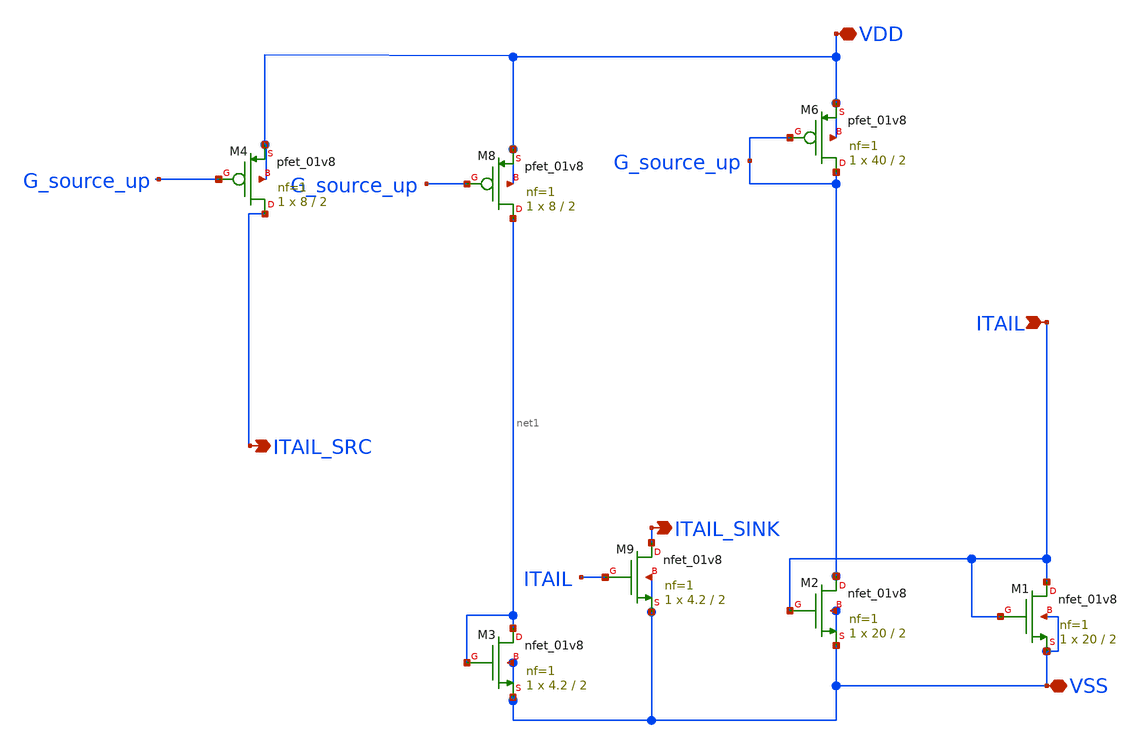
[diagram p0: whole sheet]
** sch_path: Xschem/PLL_TOP_Schematics/Current_Mirror_Top_s.sch
**.subckt Current_Mirror_Top_s ITAIL VDD VSS ITAIL_SRC ITAIL_SINK
*.ipin ITAIL
*.iopin VDD
*.iopin VSS
*.opin ITAIL_SRC
*.opin ITAIL_SINK
XM8 net1 G_source_up VDD VDD sky130_fd_pr__pfet_01v8 L=2 W=8 nf=1 ad='int((nf+1)/2) * W/nf * 0.29' as='int((nf+2)/2) * W/nf * 0.29'
+ pd='2*int((nf+1)/2) * (W/nf + 0.29)' ps='2*int((nf+2)/2) * (W/nf + 0.29)' nrd='0.29 / W' nrs='0.29 / W'
+ sa=0 sb=0 sd=0 mult=1 m=1
XM6 G_source_up G_source_up VDD VDD sky130_fd_pr__pfet_01v8 L=2 W=40 nf=1 ad='int((nf+1)/2) * W/nf * 0.29'
+ as='int((nf+2)/2) * W/nf * 0.29' pd='2*int((nf+1)/2) * (W/nf + 0.29)' ps='2*int((nf+2)/2) * (W/nf + 0.29)'
+ nrd='0.29 / W' nrs='0.29 / W' sa=0 sb=0 sd=0 mult=1 m=1
XM1 ITAIL ITAIL VSS VSS sky130_fd_pr__nfet_01v8 L=2 W=20 nf=1 ad='int((nf+1)/2) * W/nf * 0.29' as='int((nf+2)/2) * W/nf * 0.29'
+ pd='2*int((nf+1)/2) * (W/nf + 0.29)' ps='2*int((nf+2)/2) * (W/nf + 0.29)' nrd='0.29 / W' nrs='0.29 / W'
+ sa=0 sb=0 sd=0 mult=1 m=1
XM2 G_source_up ITAIL VSS VSS sky130_fd_pr__nfet_01v8 L=2 W=20 nf=1 ad='int((nf+1)/2) * W/nf * 0.29'
+ as='int((nf+2)/2) * W/nf * 0.29' pd='2*int((nf+1)/2) * (W/nf + 0.29)' ps='2*int((nf+2)/2) * (W/nf + 0.29)'
+ nrd='0.29 / W' nrs='0.29 / W' sa=0 sb=0 sd=0 mult=1 m=1
XM3 net1 net1 VSS VSS sky130_fd_pr__nfet_01v8 L=2 W=4.2 nf=1 ad='int((nf+1)/2) * W/nf * 0.29' as='int((nf+2)/2) * W/nf * 0.29'
+ pd='2*int((nf+1)/2) * (W/nf + 0.29)' ps='2*int((nf+2)/2) * (W/nf + 0.29)' nrd='0.29 / W' nrs='0.29 / W'
+ sa=0 sb=0 sd=0 mult=1 m=1
XM4 ITAIL_SRC G_source_up VDD VDD sky130_fd_pr__pfet_01v8 L=2 W=8 nf=1 ad='int((nf+1)/2) * W/nf * 0.29'
+ as='int((nf+2)/2) * W/nf * 0.29' pd='2*int((nf+1)/2) * (W/nf + 0.29)' ps='2*int((nf+2)/2) * (W/nf + 0.29)'
+ nrd='0.29 / W' nrs='0.29 / W' sa=0 sb=0 sd=0 mult=1 m=1
XM9 ITAIL_SINK ITAIL VSS VSS sky130_fd_pr__nfet_01v8 L=2 W=4.2 nf=1 ad='int((nf+1)/2) * W/nf * 0.29'
+ as='int((nf+2)/2) * W/nf * 0.29' pd='2*int((nf+1)/2) * (W/nf + 0.29)' ps='2*int((nf+2)/2) * (W/nf + 0.29)'
+ nrd='0.29 / W' nrs='0.29 / W' sa=0 sb=0 sd=0 mult=1 m=1
**.ends
.end
